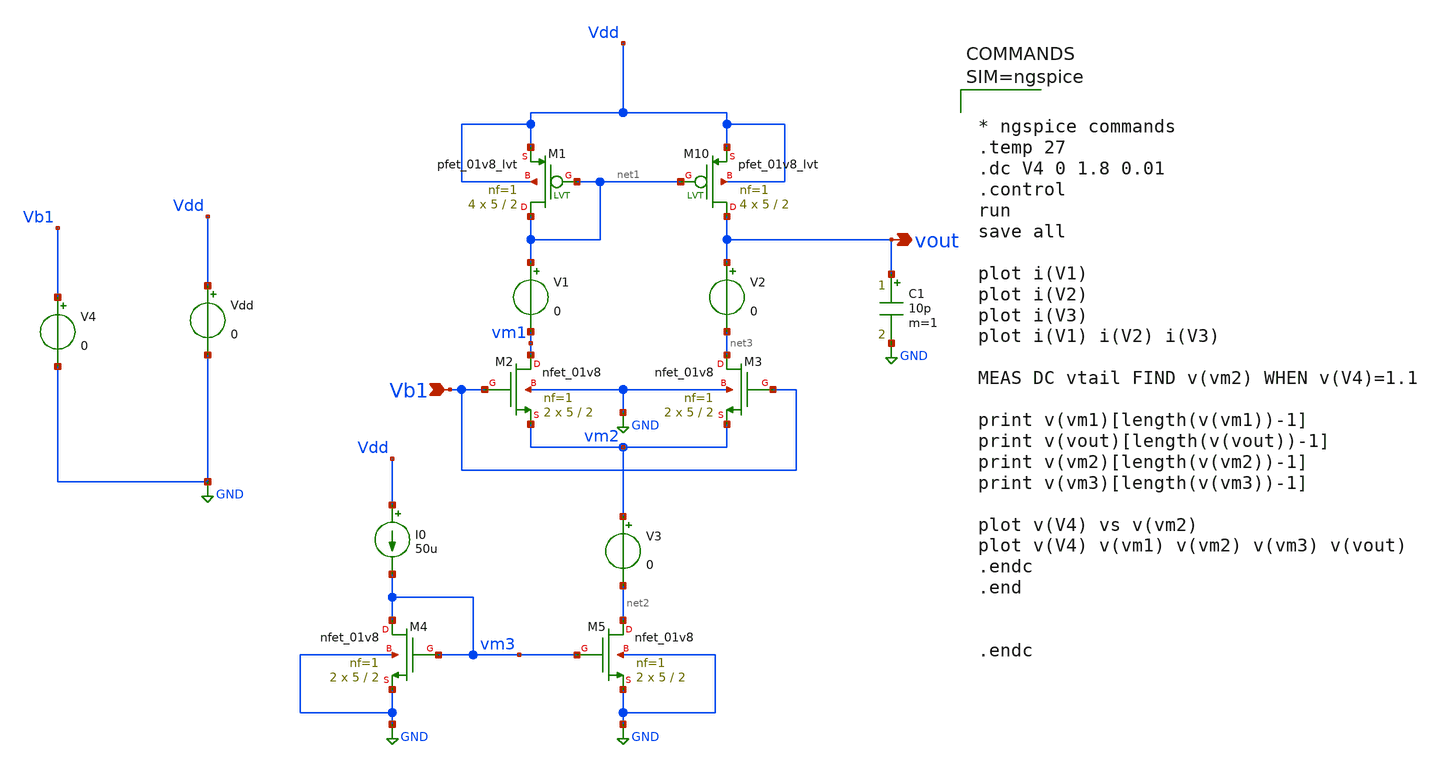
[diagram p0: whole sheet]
** sch_path: xschem/differential_ampp.sch
**.subckt differential_ampp Vb1 vout
*.ipin Vb1
*.opin vout
XM10 vout net1 Vdd Vdd sky130_fd_pr__pfet_01v8_lvt L=2 W=5 nf=1 ad='int((1 + 1)/2) * 5 / 1 * 0.29' as='int((1 + 2)/2) * 5 / 1 * 0.29'
+ pd='2*int((1 + 1)/2) * (5 / 1 + 0.29)' ps='2*int((1 + 2)/2) * (5 / 1 + 0.29)' nrd='0.29 / 5 ' nrs='0.29 / 5 '
+ sa=0 sb=0 sd=0 mult=4 m=4
XM1 net1 net1 Vdd Vdd sky130_fd_pr__pfet_01v8_lvt L=2 W=5 nf=1 ad='int((1 + 1)/2) * 5 / 1 * 0.29' as='int((1 + 2)/2) * 5 / 1 * 0.29'
+ pd='2*int((1 + 1)/2) * (5 / 1 + 0.29)' ps='2*int((1 + 2)/2) * (5 / 1 + 0.29)' nrd='0.29 / 5 ' nrs='0.29 / 5 '
+ sa=0 sb=0 sd=0 mult=4 m=4
XM2 vm1 Vb1 vm2 GND sky130_fd_pr__nfet_01v8 L=2 W=5 nf=1 ad='int((1 + 1)/2) * 5 / 1 * 0.29' as='int((1 + 2)/2) * 5 / 1 * 0.29'
+ pd='2*int((1 + 1)/2) * (5 / 1 + 0.29)' ps='2*int((1 + 2)/2) * (5 / 1 + 0.29)' nrd='0.29 / 5 ' nrs='0.29 / 5 '
+ sa=0 sb=0 sd=0 mult=2 m=2
XM3 net3 Vb1 vm2 GND sky130_fd_pr__nfet_01v8 L=2 W=5 nf=1 ad='int((1 + 1)/2) * 5 / 1 * 0.29' as='int((1 + 2)/2) * 5 / 1 * 0.29'
+ pd='2*int((1 + 1)/2) * (5 / 1 + 0.29)' ps='2*int((1 + 2)/2) * (5 / 1 + 0.29)' nrd='0.29 / 5 ' nrs='0.29 / 5 '
+ sa=0 sb=0 sd=0 mult=2 m=2
XM4 vm3 vm3 GND GND sky130_fd_pr__nfet_01v8 L=2 W=5 nf=1 ad='int((1 + 1)/2) * 5 / 1 * 0.29' as='int((1 + 2)/2) * 5 / 1 * 0.29'
+ pd='2*int((1 + 1)/2) * (5 / 1 + 0.29)' ps='2*int((1 + 2)/2) * (5 / 1 + 0.29)' nrd='0.29 / 5 ' nrs='0.29 / 5 '
+ sa=0 sb=0 sd=0 mult=2 m=2
XM5 net2 vm3 GND GND sky130_fd_pr__nfet_01v8 L=2 W=5 nf=1 ad='int((1 + 1)/2) * 5 / 1 * 0.29' as='int((1 + 2)/2) * 5 / 1 * 0.29'
+ pd='2*int((1 + 1)/2) * (5 / 1 + 0.29)' ps='2*int((1 + 2)/2) * (5 / 1 + 0.29)' nrd='0.29 / 5 ' nrs='0.29 / 5 '
+ sa=0 sb=0 sd=0 mult=2 m=2
I0 Vdd vm3 50u
C1 vout GND 10p m=1
V1 net1 vm1 0
Vdd Vdd GND 0
V4 Vb1 GND 0
V3 vm2 net2 0
V2 vout net3 0
**** begin user architecture code

** opencircuitdesign pdks install
.lib $::SKYWATER_MODELS/sky130.lib.spice tt




* ngspice commands
.temp 27
.dc V4 0 1.8 0.01
.control
run
save all

plot i(V1)
plot i(V2)
plot i(V3)
plot i(V1) i(V2) i(V3)

MEAS DC vtail FIND v(vm2) WHEN v(V4)=1.1

print v(vm1)[length(v(vm1))-1]
print v(vout)[length(v(vout))-1]
print v(vm2)[length(v(vm2))-1]
print v(vm3)[length(v(vm3))-1]

plot v(V4) vs v(vm2)
plot v(V4) v(vm1) v(vm2) v(vm3) v(vout)
.endc
.end


.endc



**** end user architecture code
**.ends
.GLOBAL GND
.end
